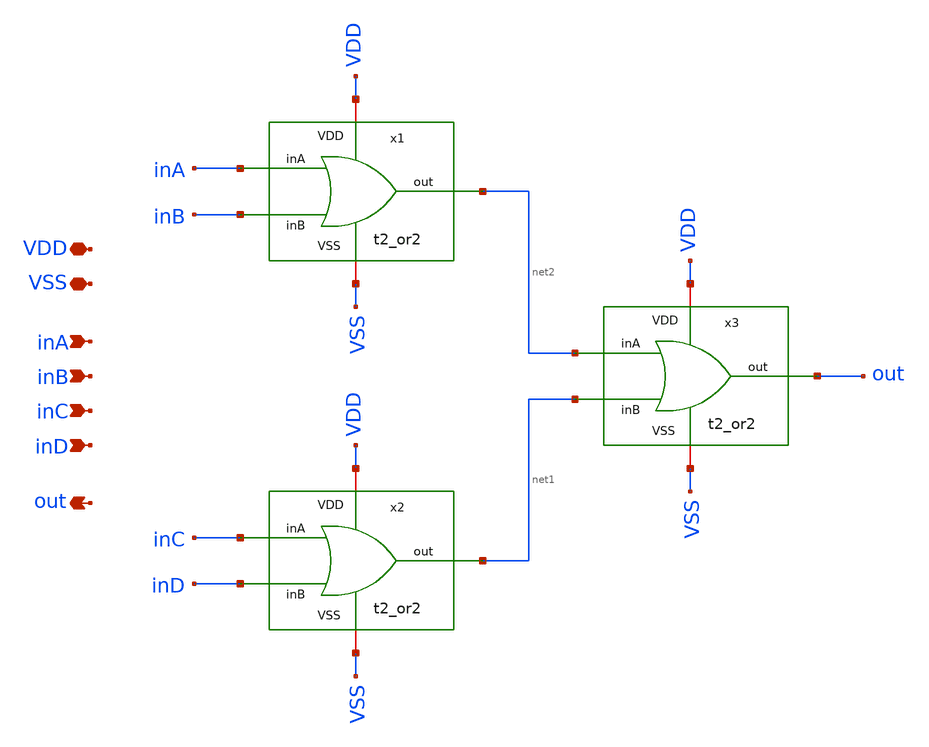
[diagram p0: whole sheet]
** sch_path: Team Designs/Team 2 Design/design_data/xschem/t2_or4.sch
**.subckt t2_or4 VSS inD out VDD inA inB inC
*.iopin VSS
*.ipin inD
*.opin out
*.iopin VDD
*.ipin inA
*.ipin inB
*.ipin inC
x1 VDD VSS inA inB net2 t2_or2
x2 VDD VSS inC inD net1 t2_or2
x3 VDD VSS net2 net1 out t2_or2
**.ends
.end
